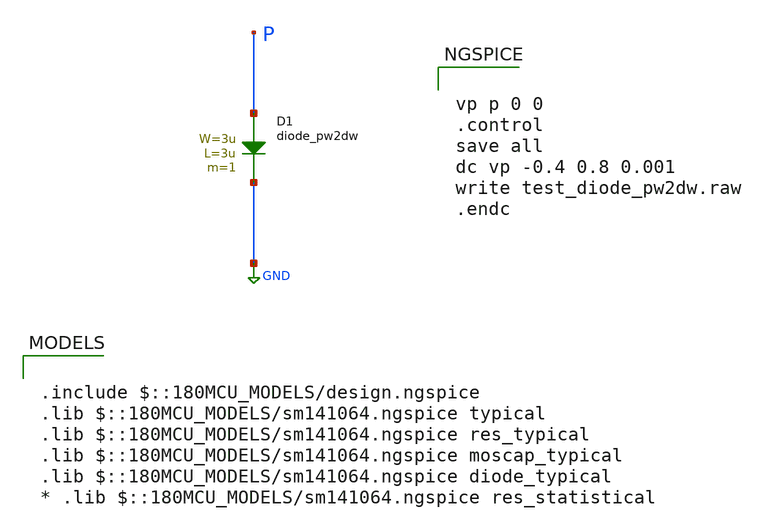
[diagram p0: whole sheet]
** sch_path: gf180mcuD/xschem_libs/gf180mcu_tests/test_diode_pw2dw/schematic/test_diode_pw2dw.sch
* Copyright 2022 GlobalFoundries PDK Authors
* Licensed under the Apache License, Version 2.0 (the "License");
* you may not use this file except in compliance with the License.
* You may obtain a copy of the License at
* https://www.apache.org/licenses/LICENSE-2.0
* Unless required by applicable law or agreed to in writing, software
* distributed under the License is distributed on an "AS IS" BASIS,
* WITHOUT WARRANTIES OR CONDITIONS OF ANY KIND, either express or implied.
* See the License for the specific language governing permissions and
* limitations under the License.
**.subckt test_diode_pw2dw
D1 P GND diode_pw2dw area='3u * 3u ' pj='2*3u + 2*3u ' m=1
**** begin user architecture code

.include $::180MCU_MODELS/design.ngspice
.lib $::180MCU_MODELS/sm141064.ngspice typical
.lib $::180MCU_MODELS/sm141064.ngspice res_typical
.lib $::180MCU_MODELS/sm141064.ngspice moscap_typical
.lib $::180MCU_MODELS/sm141064.ngspice diode_typical
* .lib $::180MCU_MODELS/sm141064.ngspice res_statistical



vp p 0 0
.control
save all
dc vp -0.4 0.8 0.001
write test_diode_pw2dw.raw
.endc


**** end user architecture code
**.ends
.GLOBAL GND
.end
